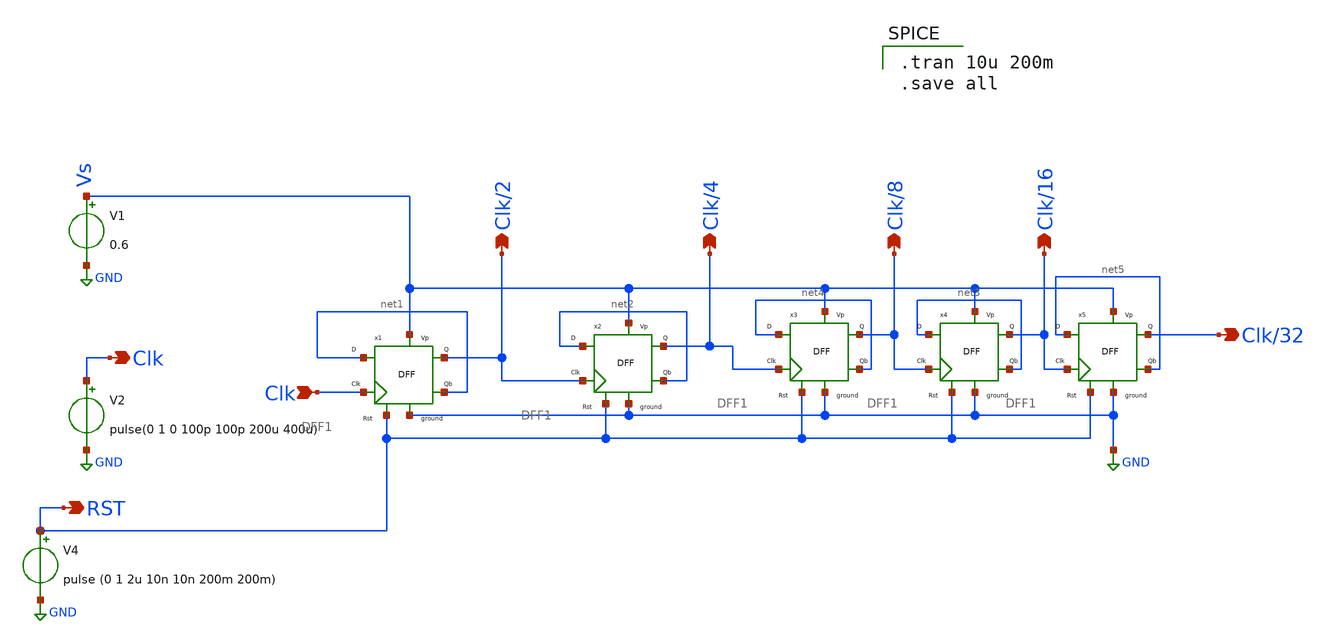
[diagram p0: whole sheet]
** sch_path: Blocks/Divide by 32 ckt/div32a.sch
**.subckt div32a Clk Clk/32 Clk RST Clk/2 Clk/4 Clk/8 Clk/16
*.opin Clk
*.opin Clk/32
*.ipin Clk
*.opin RST
*.opin Clk/2
*.opin Clk/4
*.opin Clk/8
*.opin Clk/16
V1 Vs GND 0.6
V2 Clk GND pulse(0 1 0 100p 100p 200u 400u)
V4 RST GND pulse (0 1 2u 10n 10n 200m 200m)
x1 net1 Clk RST GND Vs Clk/2 net1 DFF1
x2 net2 Clk/2 RST GND Vs Clk/4 net2 DFF1
x3 net4 Clk/4 RST GND Vs Clk/8 net4 DFF1
x4 net3 Clk/8 RST GND Vs Clk/16 net3 DFF1
x5 net5 Clk/16 RST GND Vs Clk/32 net5 DFF1
**** begin user architecture code

** opencircuitdesign pdks install
.lib $::SKYWATER_MODELS/sky130.lib.spice tt



.tran 10u 200m
.save all

**** end user architecture code
**.ends

* expanding   symbol:  component/FlipFlops/DFF1.sym # of pins=7
** sym_path: component/FlipFlops/DFF1.sym
** sch_path: component/FlipFlops/DFF1.sch
.subckt DFF1 D Clk RST VN VP Q Qb
*.opin Q
*.iopin VN
*.iopin VP
*.ipin Clk
*.ipin D
*.ipin RST
*.opin Qb
x7 net2 net4 net3 VP VN NAND
x8 net3 Clk RST VP VN net2 NAND3
x6 Q net1 RST VP VN Qb NAND3
x4 net2 Clk net4 VP VN net1 NAND3
x5 net1 D RST VP VN net4 NAND3
x1 Qb net2 Q VP VN NAND
.ends


* expanding   symbol:  component/NAND2/NAND.sym # of pins=5
** sym_path: component/NAND2/NAND.sym
** sch_path: component/NAND2/NAND.sch
.subckt NAND B A Y VP VN
*.iopin VP
*.ipin A
*.ipin B
*.opin Y
*.iopin VN
XM1 Y A VP VP sky130_fd_pr__pfet_01v8 L=0.15 W=1.26 nf=1 ad='int((nf+1)/2) * W/nf * 0.29' as='int((nf+2)/2) * W/nf * 0.29'
+ pd='2*int((nf+1)/2) * (W/nf + 0.29)' ps='2*int((nf+2)/2) * (W/nf + 0.29)' nrd='0.29 / W' nrs='0.29 / W'
+ sa=0 sb=0 sd=0 mult=1 m=1
XM2 Y B VP VP sky130_fd_pr__pfet_01v8 L=0.15 W=1.26 nf=1 ad='int((nf+1)/2) * W/nf * 0.29' as='int((nf+2)/2) * W/nf * 0.29'
+ pd='2*int((nf+1)/2) * (W/nf + 0.29)' ps='2*int((nf+2)/2) * (W/nf + 0.29)' nrd='0.29 / W' nrs='0.29 / W'
+ sa=0 sb=0 sd=0 mult=1 m=1
XM3 Y A net1 net1 sky130_fd_pr__nfet_01v8 L=0.15 W=0.84 nf=1 ad='int((nf+1)/2) * W/nf * 0.29' as='int((nf+2)/2) * W/nf * 0.29'
+ pd='2*int((nf+1)/2) * (W/nf + 0.29)' ps='2*int((nf+2)/2) * (W/nf + 0.29)' nrd='0.29 / W' nrs='0.29 / W'
+ sa=0 sb=0 sd=0 mult=1 m=1
XM4 net1 B VN VN sky130_fd_pr__nfet_01v8 L=0.15 W=0.84 nf=1 ad='int((nf+1)/2) * W/nf * 0.29' as='int((nf+2)/2) * W/nf * 0.29'
+ pd='2*int((nf+1)/2) * (W/nf + 0.29)' ps='2*int((nf+2)/2) * (W/nf + 0.29)' nrd='0.29 / W' nrs='0.29 / W'
+ sa=0 sb=0 sd=0 mult=1 m=1
.ends


* expanding   symbol:  component/NAND3/NAND3.sym # of pins=6
** sym_path: component/NAND3/NAND3.sym
** sch_path: component/NAND3/NAND3.sch
.subckt NAND3 A B C VP VN Y
*.iopin VP
*.iopin VN
*.ipin A
*.ipin B
*.ipin C
*.opin Y
XM1 Y A net1 VN sky130_fd_pr__nfet_01v8 L=0.15 W=1.26 nf=1 ad='int((nf+1)/2) * W/nf * 0.29' as='int((nf+2)/2) * W/nf * 0.29'
+ pd='2*int((nf+1)/2) * (W/nf + 0.29)' ps='2*int((nf+2)/2) * (W/nf + 0.29)' nrd='0.29 / W' nrs='0.29 / W'
+ sa=0 sb=0 sd=0 mult=1 m=1
XM2 net1 B net2 VN sky130_fd_pr__nfet_01v8 L=0.15 W=1.26 nf=1 ad='int((nf+1)/2) * W/nf * 0.29' as='int((nf+2)/2) * W/nf * 0.29'
+ pd='2*int((nf+1)/2) * (W/nf + 0.29)' ps='2*int((nf+2)/2) * (W/nf + 0.29)' nrd='0.29 / W' nrs='0.29 / W'
+ sa=0 sb=0 sd=0 mult=1 m=1
XM3 net2 C VN VN sky130_fd_pr__nfet_01v8 L=0.15 W=1.26 nf=1 ad='int((nf+1)/2) * W/nf * 0.29' as='int((nf+2)/2) * W/nf * 0.29'
+ pd='2*int((nf+1)/2) * (W/nf + 0.29)' ps='2*int((nf+2)/2) * (W/nf + 0.29)' nrd='0.29 / W' nrs='0.29 / W'
+ sa=0 sb=0 sd=0 mult=1 m=1
XM4 Y A VP VP sky130_fd_pr__pfet_01v8 L=0.15 W=1.26 nf=1 ad='int((nf+1)/2) * W/nf * 0.29' as='int((nf+2)/2) * W/nf * 0.29'
+ pd='2*int((nf+1)/2) * (W/nf + 0.29)' ps='2*int((nf+2)/2) * (W/nf + 0.29)' nrd='0.29 / W' nrs='0.29 / W'
+ sa=0 sb=0 sd=0 mult=1 m=1
XM5 Y B VP VP sky130_fd_pr__pfet_01v8 L=0.15 W=1.26 nf=1 ad='int((nf+1)/2) * W/nf * 0.29' as='int((nf+2)/2) * W/nf * 0.29'
+ pd='2*int((nf+1)/2) * (W/nf + 0.29)' ps='2*int((nf+2)/2) * (W/nf + 0.29)' nrd='0.29 / W' nrs='0.29 / W'
+ sa=0 sb=0 sd=0 mult=1 m=1
XM6 Y C VP VP sky130_fd_pr__pfet_01v8 L=0.15 W=1.26 nf=1 ad='int((nf+1)/2) * W/nf * 0.29' as='int((nf+2)/2) * W/nf * 0.29'
+ pd='2*int((nf+1)/2) * (W/nf + 0.29)' ps='2*int((nf+2)/2) * (W/nf + 0.29)' nrd='0.29 / W' nrs='0.29 / W'
+ sa=0 sb=0 sd=0 mult=1 m=1
.ends

.GLOBAL GND
.end
